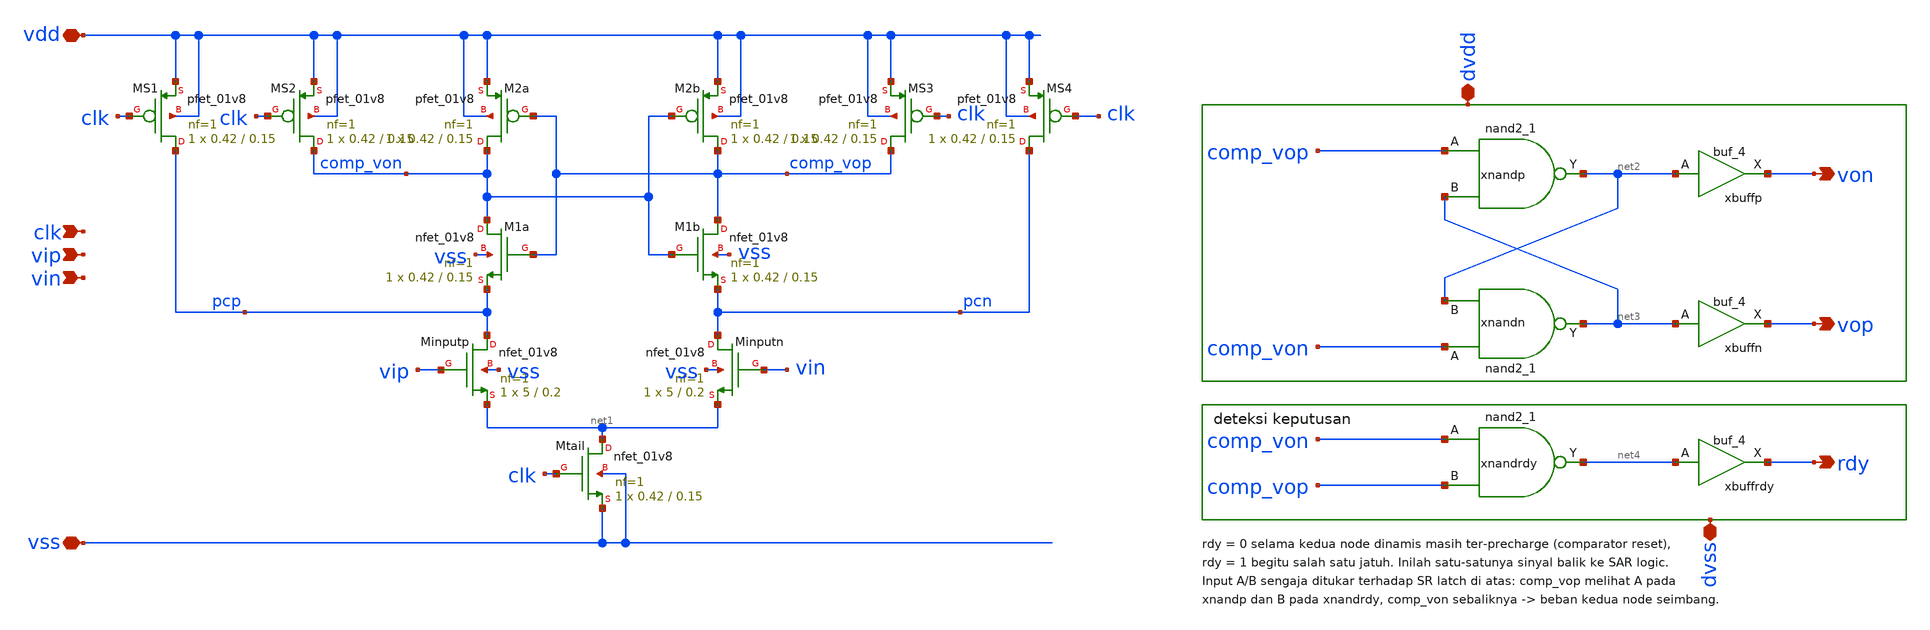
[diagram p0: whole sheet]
** sch_path: xschem/sar-adc/comparator.sch
**.subckt comparator clk vip vin vdd vss vop von dvdd dvss rdy
*.ipin clk
*.ipin vip
*.ipin vin
*.iopin vdd
*.iopin vss
*.opin vop
*.opin von
*.iopin dvdd
*.iopin dvss
*.opin rdy
XMinputp pcp vip net1 vss sky130_fd_pr__nfet_01v8 L=0.2 W=5 nf=1 ad='int((1 + 1)/2) * 5 / 1 * 0.29' as='int((1 + 2)/2) * 5 / 1 * 0.29'
+ pd='2*int((1 + 1)/2) * (5 / 1 + 0.29)' ps='2*int((1 + 2)/2) * (5 / 1 + 0.29)' nrd='0.29 / 5 ' nrs='0.29 / 5 '
+ sa=0 sb=0 sd=0 mult=1 m=1
XMinputn pcn vin net1 vss sky130_fd_pr__nfet_01v8 L=0.2 W=5 nf=1 ad='int((1 + 1)/2) * 5 / 1 * 0.29' as='int((1 + 2)/2) * 5 / 1 * 0.29'
+ pd='2*int((1 + 1)/2) * (5 / 1 + 0.29)' ps='2*int((1 + 2)/2) * (5 / 1 + 0.29)' nrd='0.29 / 5 ' nrs='0.29 / 5 '
+ sa=0 sb=0 sd=0 mult=1 m=1
XM1a comp_von comp_vop pcp vss sky130_fd_pr__nfet_01v8 L=0.15 W=0.42 nf=1 ad='int((1 + 1)/2) * 0.42 / 1 * 0.29'
+ as='int((1 + 2)/2) * 0.42 / 1 * 0.29' pd='2*int((1 + 1)/2) * (0.42 / 1 + 0.29)' ps='2*int((1 + 2)/2) * (0.42 / 1 + 0.29)'
+ nrd='0.29 / 0.42 ' nrs='0.29 / 0.42 ' sa=0 sb=0 sd=0 mult=1 m=1
XM1b comp_vop comp_von pcn vss sky130_fd_pr__nfet_01v8 L=0.15 W=0.42 nf=1 ad='int((1 + 1)/2) * 0.42 / 1 * 0.29'
+ as='int((1 + 2)/2) * 0.42 / 1 * 0.29' pd='2*int((1 + 1)/2) * (0.42 / 1 + 0.29)' ps='2*int((1 + 2)/2) * (0.42 / 1 + 0.29)'
+ nrd='0.29 / 0.42 ' nrs='0.29 / 0.42 ' sa=0 sb=0 sd=0 mult=1 m=1
XM2a comp_von comp_vop vdd vdd sky130_fd_pr__pfet_01v8 L=0.15 W=0.42 nf=1 ad='int((1 + 1)/2) * 0.42 / 1 * 0.29'
+ as='int((1 + 2)/2) * 0.42 / 1 * 0.29' pd='2*int((1 + 1)/2) * (0.42 / 1 + 0.29)' ps='2*int((1 + 2)/2) * (0.42 / 1 + 0.29)'
+ nrd='0.29 / 0.42 ' nrs='0.29 / 0.42 ' sa=0 sb=0 sd=0 mult=1 m=1
XM2b comp_vop comp_von vdd vdd sky130_fd_pr__pfet_01v8 L=0.15 W=0.42 nf=1 ad='int((1 + 1)/2) * 0.42 / 1 * 0.29'
+ as='int((1 + 2)/2) * 0.42 / 1 * 0.29' pd='2*int((1 + 1)/2) * (0.42 / 1 + 0.29)' ps='2*int((1 + 2)/2) * (0.42 / 1 + 0.29)'
+ nrd='0.29 / 0.42 ' nrs='0.29 / 0.42 ' sa=0 sb=0 sd=0 mult=1 m=1
XMtail net1 clk vss vss sky130_fd_pr__nfet_01v8 L=0.15 W=0.42 nf=1 ad='int((1 + 1)/2) * 0.42 / 1 * 0.29'
+ as='int((1 + 2)/2) * 0.42 / 1 * 0.29' pd='2*int((1 + 1)/2) * (0.42 / 1 + 0.29)' ps='2*int((1 + 2)/2) * (0.42 / 1 + 0.29)'
+ nrd='0.29 / 0.42 ' nrs='0.29 / 0.42 ' sa=0 sb=0 sd=0 mult=1 m=1
XMS3 comp_vop clk vdd vdd sky130_fd_pr__pfet_01v8 L=0.15 W=0.42 nf=1 ad='int((1 + 1)/2) * 0.42 / 1 * 0.29'
+ as='int((1 + 2)/2) * 0.42 / 1 * 0.29' pd='2*int((1 + 1)/2) * (0.42 / 1 + 0.29)' ps='2*int((1 + 2)/2) * (0.42 / 1 + 0.29)'
+ nrd='0.29 / 0.42 ' nrs='0.29 / 0.42 ' sa=0 sb=0 sd=0 mult=1 m=1
XMS2 comp_von clk vdd vdd sky130_fd_pr__pfet_01v8 L=0.15 W=0.42 nf=1 ad='int((1 + 1)/2) * 0.42 / 1 * 0.29'
+ as='int((1 + 2)/2) * 0.42 / 1 * 0.29' pd='2*int((1 + 1)/2) * (0.42 / 1 + 0.29)' ps='2*int((1 + 2)/2) * (0.42 / 1 + 0.29)'
+ nrd='0.29 / 0.42 ' nrs='0.29 / 0.42 ' sa=0 sb=0 sd=0 mult=1 m=1
XMS4 pcn clk vdd vdd sky130_fd_pr__pfet_01v8 L=0.15 W=0.42 nf=1 ad='int((1 + 1)/2) * 0.42 / 1 * 0.29'
+ as='int((1 + 2)/2) * 0.42 / 1 * 0.29' pd='2*int((1 + 1)/2) * (0.42 / 1 + 0.29)' ps='2*int((1 + 2)/2) * (0.42 / 1 + 0.29)'
+ nrd='0.29 / 0.42 ' nrs='0.29 / 0.42 ' sa=0 sb=0 sd=0 mult=1 m=1
XMS1 pcp clk vdd vdd sky130_fd_pr__pfet_01v8 L=0.15 W=0.42 nf=1 ad='int((1 + 1)/2) * 0.42 / 1 * 0.29'
+ as='int((1 + 2)/2) * 0.42 / 1 * 0.29' pd='2*int((1 + 1)/2) * (0.42 / 1 + 0.29)' ps='2*int((1 + 2)/2) * (0.42 / 1 + 0.29)'
+ nrd='0.29 / 0.42 ' nrs='0.29 / 0.42 ' sa=0 sb=0 sd=0 mult=1 m=1
xnandp comp_vop net3 dvss dvss dvdd dvdd net2 sky130_fd_sc_hd__nand2_1
xnandn comp_von net2 dvss dvss dvdd dvdd net3 sky130_fd_sc_hd__nand2_1
xbuffp net2 dvss dvss dvdd dvdd von sky130_fd_sc_hd__buf_4
xbuffn net3 dvss dvss dvdd dvdd vop sky130_fd_sc_hd__buf_4
xnandrdy comp_von comp_vop dvss dvss dvdd dvdd net4 sky130_fd_sc_hd__nand2_1
xbuffrdy net4 dvss dvss dvdd dvdd rdy sky130_fd_sc_hd__buf_4
**.ends
.end
